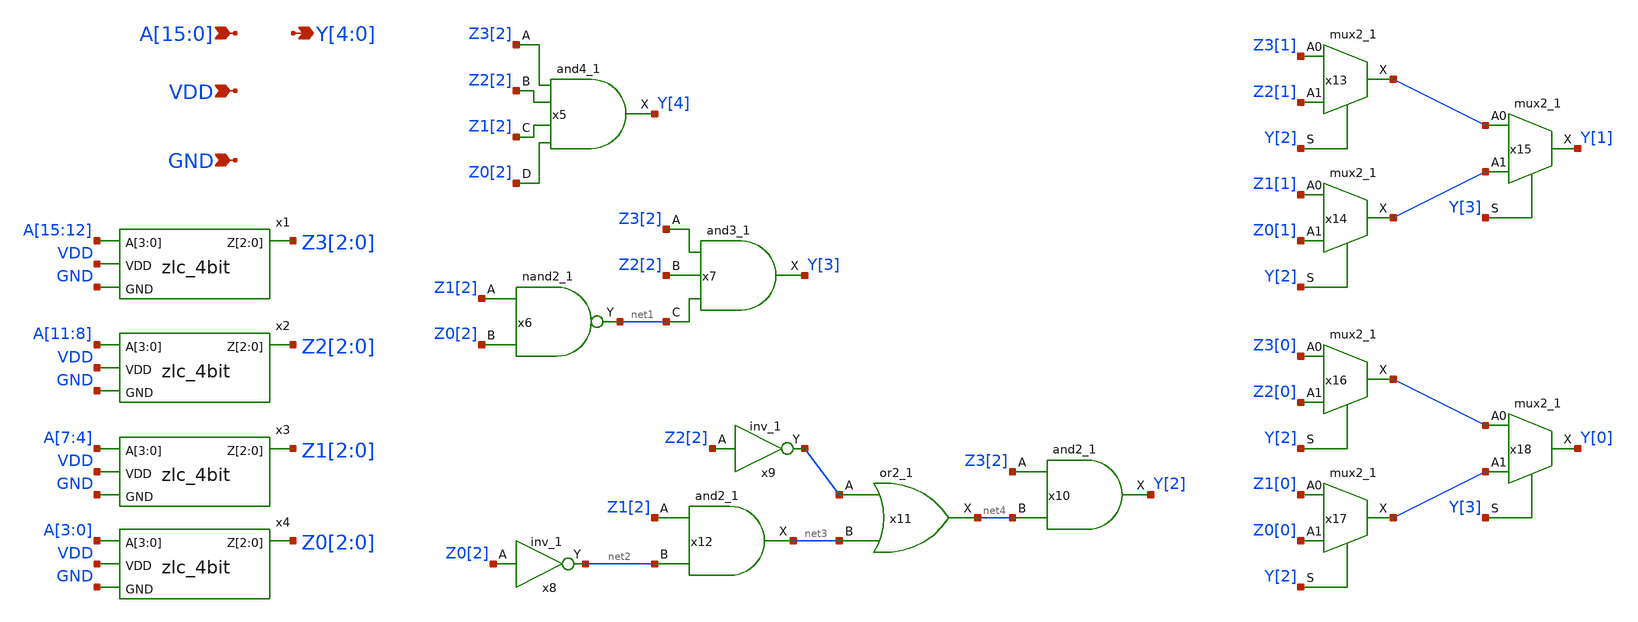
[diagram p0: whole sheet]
** sch_path: xschem/zlc_16bit.sch
**.subckt zlc_16bit VDD GND
*+ A[15],A[14],A[13],A[12],A[11],A[10],A[9],A[8],A[7],A[6],A[5],A[4],A[3],A[2],A[1],A[0] Y[4],Y[3],Y[2],Y[1],Y[0]
*.ipin VDD
*.ipin GND
*.ipin A[15],A[14],A[13],A[12],A[11],A[10],A[9],A[8],A[7],A[6],A[5],A[4],A[3],A[2],A[1],A[0]
*.opin Y[4],Y[3],Y[2],Y[1],Y[0]
x5 Z3[2] Z2[2] Z1[2] Z0[2] GND GND VDD VDD Y[4] sky130_fd_sc_hd__and4_1
x6 Z1[2] Z0[2] GND GND VDD VDD net1 sky130_fd_sc_hd__nand2_1
x7 Z3[2] Z2[2] net1 GND GND VDD VDD Y[3] sky130_fd_sc_hd__and3_1
x8 Z0[2] GND GND VDD VDD net2 sky130_fd_sc_hd__inv_1
x9 Z2[2] GND GND VDD VDD net5 sky130_fd_sc_hd__inv_1
x10 Z3[2] net4 GND GND VDD VDD Y[2] sky130_fd_sc_hd__and2_1
x11 net5 net3 GND GND VDD VDD net4 sky130_fd_sc_hd__or2_1
x12 Z1[2] net2 GND GND VDD VDD net3 sky130_fd_sc_hd__and2_1
x13 Z3[1] Z2[1] Y[2] GND GND VDD VDD net6 sky130_fd_sc_hd__mux2_1
x14 Z1[1] Z0[1] Y[2] GND GND VDD VDD net7 sky130_fd_sc_hd__mux2_1
x15 net6 net7 Y[3] GND GND VDD VDD Y[1] sky130_fd_sc_hd__mux2_1
x16 Z3[0] Z2[0] Y[2] GND GND VDD VDD net8 sky130_fd_sc_hd__mux2_1
x17 Z1[0] Z0[0] Y[2] GND GND VDD VDD net9 sky130_fd_sc_hd__mux2_1
x18 net8 net9 Y[3] GND GND VDD VDD Y[0] sky130_fd_sc_hd__mux2_1
x1 Z3[2] Z3[1] Z3[0] A[15] A[14] A[13] A[12] VDD GND zlc_4bit
x2 Z2[2] Z2[1] Z2[0] A[11] A[10] A[9] A[8] VDD GND zlc_4bit
x3 Z1[2] Z1[1] Z1[0] A[7] A[6] A[5] A[4] VDD GND zlc_4bit
x4 Z0[2] Z0[1] Z0[0] A[3] A[2] A[1] A[0] VDD GND zlc_4bit
**.ends

* expanding   symbol:  zlc_4bit.sym # of pins=4
** sym_path: xschem/zlc_4bit.sym
** sch_path: xschem/zlc_4bit.sch
.subckt zlc_4bit Z[2] Z[1] Z[0] A[3] A[2] A[1] A[0] VDD GND
*.ipin A[3],A[2],A[1],A[0]
*.opin Z[2],Z[1],Z[0]
*.ipin VDD
*.ipin GND
x1 A[3] A[2] A[1] A[0] GND GND VDD VDD Z[2] sky130_fd_sc_hd__nor4_1
x2 A[3] A[2] GND GND VDD VDD net5 sky130_fd_sc_hd__nor2_1
x3 A[1] A[0] GND GND VDD VDD net6 sky130_fd_sc_hd__or2_1
x4 net5 net6 GND GND VDD VDD Z[1] sky130_fd_sc_hd__and2_1
x5 A[3] GND GND VDD VDD net4 sky130_fd_sc_hd__inv_1
x7 net1 A[0] GND GND VDD VDD net2 sky130_fd_sc_hd__and2_1
x8 net2 A[2] GND GND VDD VDD net3 sky130_fd_sc_hd__or2_1
x9 net4 net3 GND GND VDD VDD Z[0] sky130_fd_sc_hd__and2_1
x6 A[1] GND GND VDD VDD net1 sky130_fd_sc_hd__inv_1
.ends

.end
